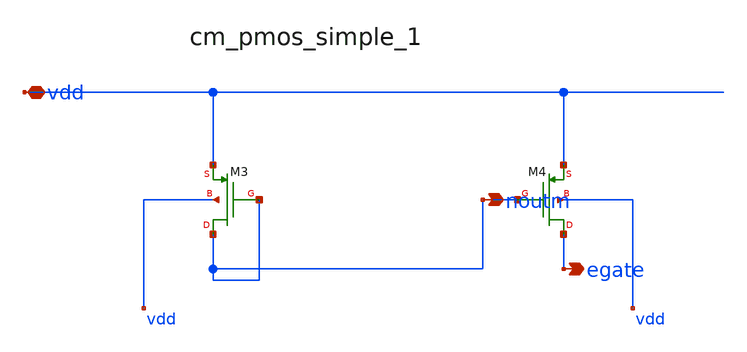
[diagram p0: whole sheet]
** sch_path: analog-db/raw/ldo_007_pmos/hier/blocks/cm_pmos_simple_1.sch
**.subckt cm_pmos_simple_1 vdd noutm egate
*.iopin vdd
*.opin noutm
*.opin egate
XM3 noutm noutm vdd vdd sg13_lv_pmos w=x_dut_xm3_w l=x_dut_xm3_l ng=1 m=1
XM4 egate noutm vdd vdd sg13_lv_pmos w=x_dut_xm4_w l=x_dut_xm4_l ng=1 m=1
**.ends
.end
